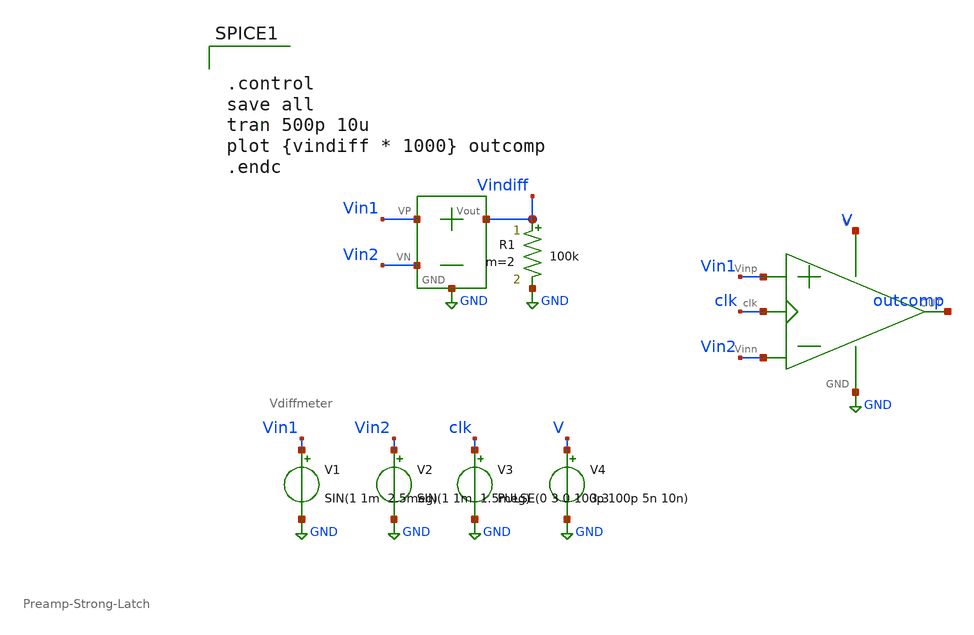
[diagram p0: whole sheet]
** sch_path: testbench/comp_full_tb/100mv_sin_1meg-200mv_sin_2meg__tb.sch
**.subckt 100mv_sin_1meg-200mv_sin_2meg__tb
X1 V GND Vin1 Vin2 outcomp clk Preamp-Strong-Latch
V1 Vin1 GND SIN(1 1m 2.5meg)
V2 Vin2 GND SIN(1 1m 1.5meg)
V3 clk GND PULSE(0 3 0 100p 100p 5n 10n)
V4 V GND 3.3
X2 Vin1 Vin2 Vindiff GND Vdiffmeter
R1 Vindiff GND 100k m=2
**** begin user architecture code


.control
save all
tran 500p 10u
plot {vindiff * 1000} outcomp
.endc


.include /foss/pdks/gf180mcuC/libs.tech/ngspice/design.ngspice
.lib /foss/pdks/gf180mcuC/libs.tech/ngspice/sm141064.ngspice typical

**** end user architecture code
**.ends
.GLOBAL GND
.end
